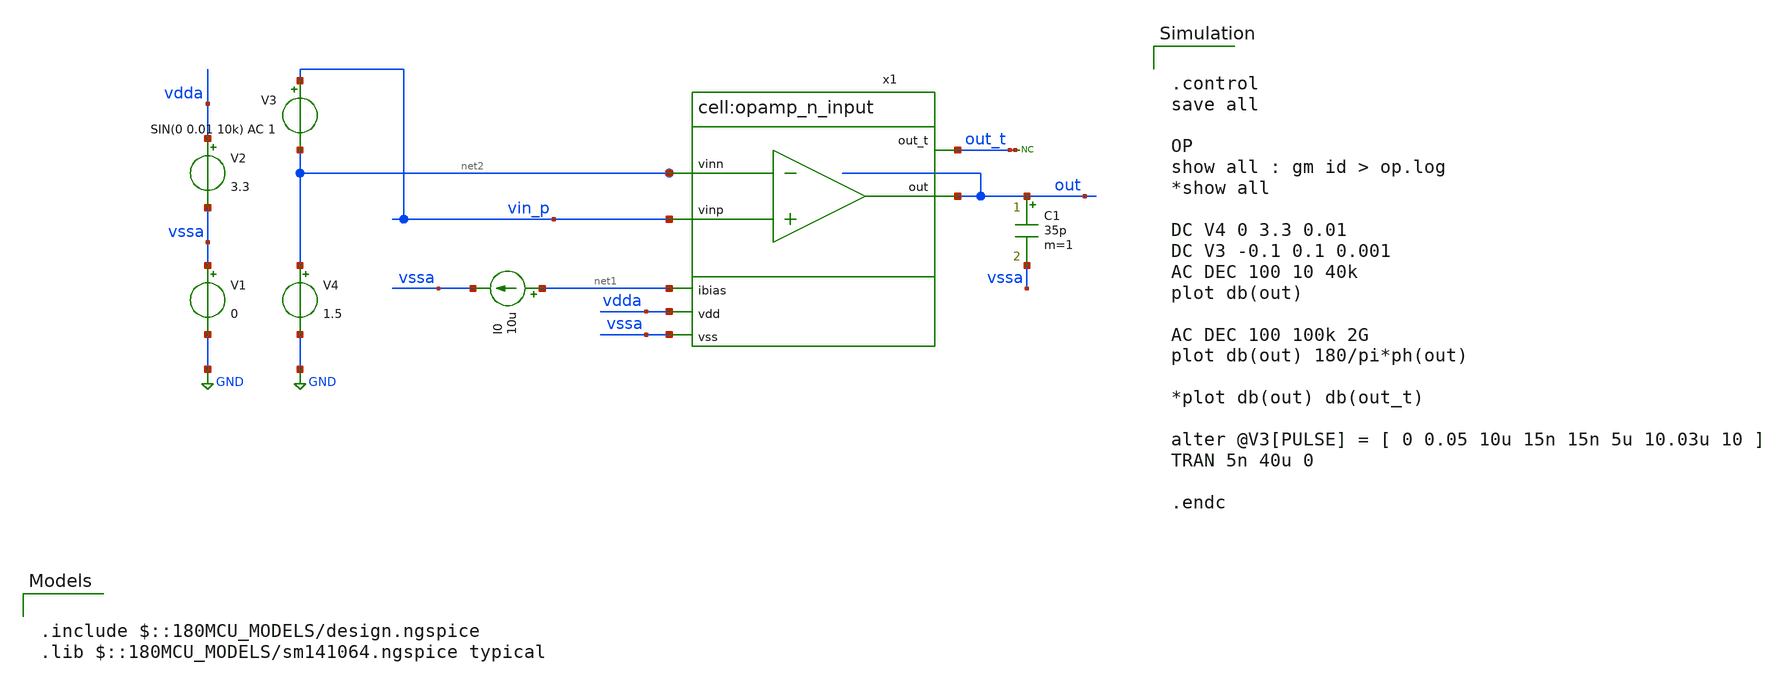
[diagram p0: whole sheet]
** sch_path: designs/libs/tb_analog/opamp/opamp_n_tb.sch
**.subckt opamp_n_tb
x1 vin_p net2 net1 vdda out vssa out_t opamp_n_input
V1 vssa GND 0
V2 vdda vssa 3.3
I0 net1 vssa 10u
V3 vin_p net2 SIN(0 0.01 10k) AC 1
V4 net2 GND 1.5
C1 out vssa 35p m=1
* noconn out_t
**** begin user architecture code


.control
save all

OP
show all : gm id > op.log
*show all

DC V4 0 3.3 0.01
DC V3 -0.1 0.1 0.001
AC DEC 100 10 40k
plot db(out)

AC DEC 100 100k 2G
plot db(out) 180/pi*ph(out)

*plot db(out) db(out_t)

alter @V3[PULSE] = [ 0 0.05 10u 15n 15n 5u 10.03u 10 ]
TRAN 5n 40u 0

.endc



.include $::180MCU_MODELS/design.ngspice
.lib $::180MCU_MODELS/sm141064.ngspice typical

**** end user architecture code
**.ends
.GLOBAL GND
.end
